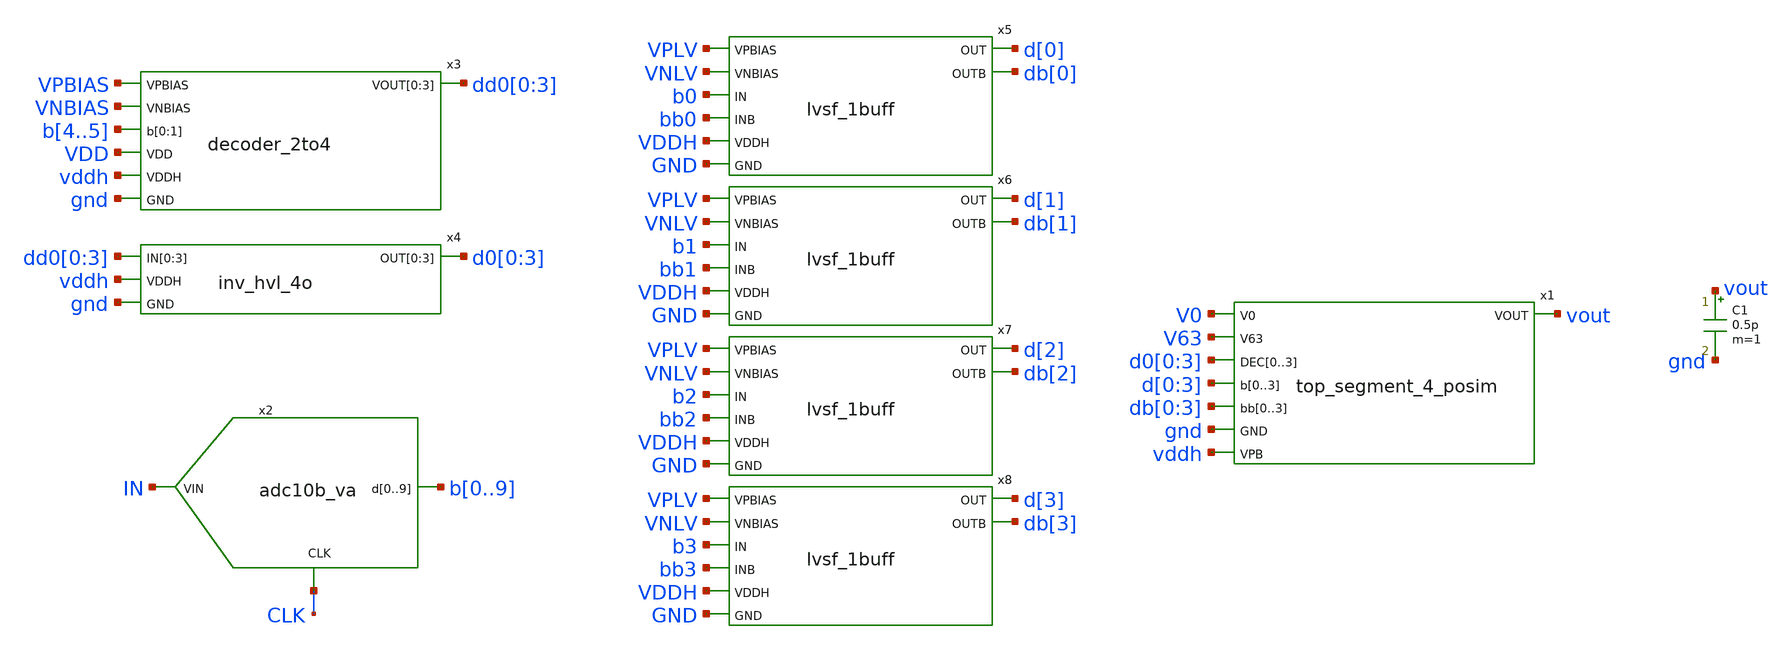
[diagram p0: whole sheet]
** sch_path: xschem/res_seg_4-tb.sch
.lib $::SKYWATER_MODELS/sky130.lib.spice tt
.include $::SKYWATER_STDCELLS/sky130_fd_sc_hd.spice

**.subckt res_seg_4-tb
x3 VPBIAS VNBIAS b4 b5 dd0[0] dd0[1] dd0[2] dd0[3] VDD vddh gnd decoder_2to4
x5 VPLV VNLV b0 bb0 d[0] db[0] VDDH GND lvsf_1buff
x6 VPLV VNLV b1 bb1 d[1] db[1] VDDH GND lvsf_1buff
x7 VPLV VNLV b2 bb2 d[2] db[2] VDDH GND lvsf_1buff
x8 VPLV VNLV b3 bb3 d[3] db[3] VDDH GND lvsf_1buff
x4 dd0[0] dd0[1] dd0[2] dd0[3] d0[0] d0[1] d0[2] d0[3] vddh gnd inv_hvl_4o
C1 vout gnd 0.5p m=1
x1 V0 V63 d0[0] d0[1] d0[2] d0[3] d[0] d[1] d[2] d[3] db[0] db[1] db[2] db[3] vout gnd vddh
+ top_segment_4_posim
x2 IN CLK b0 b1 b2 b3 b4 b5 b6 b7 b8 b9 adc10b_va
**** begin user architecture code


.include $THESIS_WS/spice/rseg_4_tb.sp
.save vout b0 b1 b2 b3 b4 b5
.save bb0 bb1 bb2 bb3 bb4 bb5



**** end user architecture code
**.ends

* expanding   symbol:  decoder_2to4.sym # of pins=7
** sym_path: xschem/decoder_2to4.sym
** sch_path: xschem/decoder_2to4.sch
.subckt decoder_2to4 VPBIAS VNBIAS b[0] b[1] VOUT[0] VOUT[1] VOUT[2] VOUT[3] VDD VDDH GND
*.ipin VPBIAS
*.ipin VNBIAS
*.ipin b[0],b[1]
*.opin VOUT[0],VOUT[1],VOUT[2],VOUT[3]
*.ipin VDDH
*.ipin GND
*.ipin VDD
x1 VPBIAS VNBIAS DIN[0] VOUT[1] VOUT[2] VOUT[3] VOUT[0] VDDH GND VDDH GND pull_up_down_network
x2 VPBIAS VNBIAS DIN[1] VOUT[0] VOUT[2] VOUT[3] VOUT[1] VDDH GND VDDH GND pull_up_down_network
x3 VPBIAS VNBIAS DIN[2] VOUT[0] VOUT[1] VOUT[3] VOUT[2] VDDH GND VDDH GND pull_up_down_network
x4 VPBIAS VNBIAS DIN[3] VOUT[0] VOUT[1] VOUT[2] VOUT[3] VDDH GND VDDH GND pull_up_down_network
x6 bb[0] bb[1] DIN[0] VDD GND nand
x7 b[0] bb[1] DIN[1] VDD GND nand
x8 bb[0] b[1] DIN[2] VDD GND nand
x9 b[0] b[1] DIN[3] VDD GND nand
x5 b[0] bb[0] VDD GND inv
x10 b[1] bb[1] VDD GND inv
.ends


* expanding   symbol:  lvsf_1buff.sym # of pins=8
** sym_path: xschem/lvsf_1buff.sym
** sch_path: xschem/lvsf_1buff.sch
.subckt lvsf_1buff VPBIAS VNBIAS IN INB OUT OUTB VDDH GND
*.ipin IN
*.ipin INB
*.opin OUT
*.ipin VDDH
*.ipin GND
*.ipin VPBIAS
*.ipin VNBIAS
*.opin OUTB
XM13 n1 IN GND GND sky130_fd_pr__nfet_01v8 L=0.15 W=3 nf=1 ad='int((nf+1)/2) * W/nf * 0.29' as='int((nf+2)/2) * W/nf * 0.29'
+ pd='2*int((nf+1)/2) * (W/nf + 0.29)' ps='2*int((nf+2)/2) * (W/nf + 0.29)' nrd='0.29 / W' nrs='0.29 / W'
+ sa=0 sb=0 sd=0 mult=1 m=1
XM1 net2 VPBIAS VDDH VDDH sky130_fd_pr__pfet_g5v0d10v5 L=0.8 W=1 nf=1 ad='int((nf+1)/2) * W/nf * 0.29'
+ as='int((nf+2)/2) * W/nf * 0.29' pd='2*int((nf+1)/2) * (W/nf + 0.29)' ps='2*int((nf+2)/2) * (W/nf + 0.29)'
+ nrd='0.29 / W' nrs='0.29 / W' sa=0 sb=0 sd=0 mult=1 m=1
XM2 net1 VPBIAS VDDH VDDH sky130_fd_pr__pfet_g5v0d10v5 L=0.8 W=1 nf=1 ad='int((nf+1)/2) * W/nf * 0.29'
+ as='int((nf+2)/2) * W/nf * 0.29' pd='2*int((nf+1)/2) * (W/nf + 0.29)' ps='2*int((nf+2)/2) * (W/nf + 0.29)'
+ nrd='0.29 / W' nrs='0.29 / W' sa=0 sb=0 sd=0 mult=1 m=1
XM3 OUTPB OUTP net2 VDDH sky130_fd_pr__pfet_g5v0d10v5 L=0.8 W=1 nf=1 ad='int((nf+1)/2) * W/nf * 0.29'
+ as='int((nf+2)/2) * W/nf * 0.29' pd='2*int((nf+1)/2) * (W/nf + 0.29)' ps='2*int((nf+2)/2) * (W/nf + 0.29)'
+ nrd='0.29 / W' nrs='0.29 / W' sa=0 sb=0 sd=0 mult=1 m=1
XM4 OUTP OUTPB net1 VDDH sky130_fd_pr__pfet_g5v0d10v5 L=0.8 W=1 nf=1 ad='int((nf+1)/2) * W/nf * 0.29'
+ as='int((nf+2)/2) * W/nf * 0.29' pd='2*int((nf+1)/2) * (W/nf + 0.29)' ps='2*int((nf+2)/2) * (W/nf + 0.29)'
+ nrd='0.29 / W' nrs='0.29 / W' sa=0 sb=0 sd=0 mult=1 m=1
XM5 OUTPB VNBIAS n1 GND sky130_fd_pr__nfet_g5v0d10v5 L=1 W=1 nf=1 ad='int((nf+1)/2) * W/nf * 0.29' as='int((nf+2)/2) * W/nf * 0.29'
+ pd='2*int((nf+1)/2) * (W/nf + 0.29)' ps='2*int((nf+2)/2) * (W/nf + 0.29)' nrd='0.29 / W' nrs='0.29 / W'
+ sa=0 sb=0 sd=0 mult=1 m=1
XM6 OUTP VNBIAS n2 GND sky130_fd_pr__nfet_g5v0d10v5 L=1 W=1 nf=1 ad='int((nf+1)/2) * W/nf * 0.29' as='int((nf+2)/2) * W/nf * 0.29'
+ pd='2*int((nf+1)/2) * (W/nf + 0.29)' ps='2*int((nf+2)/2) * (W/nf + 0.29)' nrd='0.29 / W' nrs='0.29 / W'
+ sa=0 sb=0 sd=0 mult=1 m=1
XM7 n2 INB GND GND sky130_fd_pr__nfet_01v8 L=0.15 W=3 nf=1 ad='int((nf+1)/2) * W/nf * 0.29' as='int((nf+2)/2) * W/nf * 0.29'
+ pd='2*int((nf+1)/2) * (W/nf + 0.29)' ps='2*int((nf+2)/2) * (W/nf + 0.29)' nrd='0.29 / W' nrs='0.29 / W'
+ sa=0 sb=0 sd=0 mult=1 m=1
x1 OUTP GND GND VDDH VDDH OUTB sky130_fd_sc_hvl__inv_1
x2 OUTB GND GND VDDH VDDH OUT sky130_fd_sc_hvl__inv_1
.ends


* expanding   symbol:  inv_hvl_4o.sym # of pins=4
** sym_path: xschem/inv_hvl_4o.sym
** sch_path: xschem/inv_hvl_4o.sch
.subckt inv_hvl_4o IN[0] IN[1] IN[2] IN[3] OUT[0] OUT[1] OUT[2] OUT[3] VDDH GND
*.ipin IN[0],IN[1],IN[2],IN[3]
*.opin OUT[0],OUT[1],OUT[2],OUT[3]
*.ipin VDDH
*.ipin GND
x1 IN[0] GND GND VDDH VDDH OUT[0] sky130_fd_sc_hd__inv_1
x2 IN[1] GND GND VDDH VDDH OUT[1] sky130_fd_sc_hd__inv_1
x3 IN[2] GND GND VDDH VDDH OUT[2] sky130_fd_sc_hd__inv_1
x4 IN[3] GND GND VDDH VDDH OUT[3] sky130_fd_sc_hd__inv_1
.ends


* expanding   symbol:  pull_up_down_network.sym # of pins=9
** sym_path: xschem/pull_up_down_network.sym
** sch_path: xschem/pull_up_down_network.sch
.subckt pull_up_down_network VPBIAS VNBIAS DIN V[0] V[1] V[2] VOUT VDDH GND VPB VNB
*.ipin VPBIAS
*.ipin VNBIAS
*.ipin DIN
*.ipin V[0],V[1],V[2]
*.opin VOUT
*.ipin VDDH
*.ipin GND
*.ipin VPB
*.ipin VNB
XM1 net2 VPBIAS VDDH VPB sky130_fd_pr__pfet_g5v0d10v5 L=l W=wp nf=1 ad='int((nf+1)/2) * W/nf * 0.29'
+ as='int((nf+2)/2) * W/nf * 0.29' pd='2*int((nf+1)/2) * (W/nf + 0.29)' ps='2*int((nf+2)/2) * (W/nf + 0.29)'
+ nrd='0.29 / W' nrs='0.29 / W' sa=0 sb=0 sd=0 mult=1 m=1
.param wp=0.84 wn=1 l=1

XM2 net3 V[0] net2 VPB sky130_fd_pr__pfet_g5v0d10v5 L=l W=wp nf=1 ad='int((nf+1)/2) * W/nf * 0.29' as='int((nf+2)/2) * W/nf * 0.29'
+ pd='2*int((nf+1)/2) * (W/nf + 0.29)' ps='2*int((nf+2)/2) * (W/nf + 0.29)' nrd='0.29 / W' nrs='0.29 / W'
+ sa=0 sb=0 sd=0 mult=1 m=1
XM3 net4 V[1] net3 VPB sky130_fd_pr__pfet_g5v0d10v5 L=l W=wp nf=1 ad='int((nf+1)/2) * W/nf * 0.29' as='int((nf+2)/2) * W/nf * 0.29'
+ pd='2*int((nf+1)/2) * (W/nf + 0.29)' ps='2*int((nf+2)/2) * (W/nf + 0.29)' nrd='0.29 / W' nrs='0.29 / W'
+ sa=0 sb=0 sd=0 mult=1 m=1
XM4 VOUT V[2] net4 VPB sky130_fd_pr__pfet_g5v0d10v5 L=l W=wp nf=1 ad='int((nf+1)/2) * W/nf * 0.29' as='int((nf+2)/2) * W/nf * 0.29'
+ pd='2*int((nf+1)/2) * (W/nf + 0.29)' ps='2*int((nf+2)/2) * (W/nf + 0.29)' nrd='0.29 / W' nrs='0.29 / W'
+ sa=0 sb=0 sd=0 mult=1 m=1
XM5 VOUT VNBIAS net1 VNB sky130_fd_pr__nfet_g5v0d10v5 L=l W=wn nf=1 ad='int((nf+1)/2) * W/nf * 0.29'
+ as='int((nf+2)/2) * W/nf * 0.29' pd='2*int((nf+1)/2) * (W/nf + 0.29)' ps='2*int((nf+2)/2) * (W/nf + 0.29)'
+ nrd='0.29 / W' nrs='0.29 / W' sa=0 sb=0 sd=0 mult=1 m=1
XM6 net1 DIN GND VNB sky130_fd_pr__nfet_01v8 L=0.15 W=2 nf=1 ad='int((nf+1)/2) * W/nf * 0.29' as='int((nf+2)/2) * W/nf * 0.29'
+ pd='2*int((nf+1)/2) * (W/nf + 0.29)' ps='2*int((nf+2)/2) * (W/nf + 0.29)' nrd='0.29 / W' nrs='0.29 / W'
+ sa=0 sb=0 sd=0 mult=1 m=1
.ends


* expanding   symbol:  nand.sym # of pins=5
** sym_path: xschem/nand.sym
** sch_path: xschem/nand.sch
.subckt nand in1 in2 out VDD GND
*.ipin in2
*.opin out
*.ipin VDD
*.ipin GND
*.ipin in1
.param wp=0.63 wn=0.42 l=0.15
XM1 out in1 VDD VDD sky130_fd_pr__pfet_01v8 L=l W=wp nf=1 ad='int((nf+1)/2) * W/nf * 0.29' as='int((nf+2)/2) * W/nf * 0.29'
+ pd='2*int((nf+1)/2) * (W/nf + 0.29)' ps='2*int((nf+2)/2) * (W/nf + 0.29)' nrd='0.29 / W' nrs='0.29 / W'
+ sa=0 sb=0 sd=0 mult=1 m=1
XM2 out in2 VDD VDD sky130_fd_pr__pfet_01v8 L=l W=wp nf=1 ad='int((nf+1)/2) * W/nf * 0.29' as='int((nf+2)/2) * W/nf * 0.29'
+ pd='2*int((nf+1)/2) * (W/nf + 0.29)' ps='2*int((nf+2)/2) * (W/nf + 0.29)' nrd='0.29 / W' nrs='0.29 / W'
+ sa=0 sb=0 sd=0 mult=1 m=1
XM3 out in2 net1 GND sky130_fd_pr__nfet_01v8 L=l W=wn nf=1 ad='int((nf+1)/2) * W/nf * 0.29' as='int((nf+2)/2) * W/nf * 0.29'
+ pd='2*int((nf+1)/2) * (W/nf + 0.29)' ps='2*int((nf+2)/2) * (W/nf + 0.29)' nrd='0.29 / W' nrs='0.29 / W'
+ sa=0 sb=0 sd=0 mult=1 m=1
XM4 net1 in1 GND GND sky130_fd_pr__nfet_01v8 L=l W=wn nf=1 ad='int((nf+1)/2) * W/nf * 0.29' as='int((nf+2)/2) * W/nf * 0.29'
+ pd='2*int((nf+1)/2) * (W/nf + 0.29)' ps='2*int((nf+2)/2) * (W/nf + 0.29)' nrd='0.29 / W' nrs='0.29 / W'
+ sa=0 sb=0 sd=0 mult=1 m=1
.ends


* expanding   symbol:  inv.sym # of pins=4
** sym_path: xschem/inv.sym
** sch_path: xschem/inv.sch
.subckt inv in out vdd gnd
*.ipin in
*.opin out
*.ipin vdd
*.ipin gnd
XM1 out in gnd gnd sky130_fd_pr__nfet_01v8 L=0.15 W=0.42 nf=1 ad='int((nf+1)/2) * W/nf * 0.29' as='int((nf+2)/2) * W/nf * 0.29'
+ pd='2*int((nf+1)/2) * (W/nf + 0.29)' ps='2*int((nf+2)/2) * (W/nf + 0.29)' nrd='0.29 / W' nrs='0.29 / W'
+ sa=0 sb=0 sd=0 mult=1 m=1
XM2 out in vdd vdd sky130_fd_pr__pfet_01v8 L=0.15 W=1.26 nf=1 ad='int((nf+1)/2) * W/nf * 0.29' as='int((nf+2)/2) * W/nf * 0.29'
+ pd='2*int((nf+1)/2) * (W/nf + 0.29)' ps='2*int((nf+2)/2) * (W/nf + 0.29)' nrd='0.29 / W' nrs='0.29 / W'
+ sa=0 sb=0 sd=0 mult=1 m=1
.ends

.end
